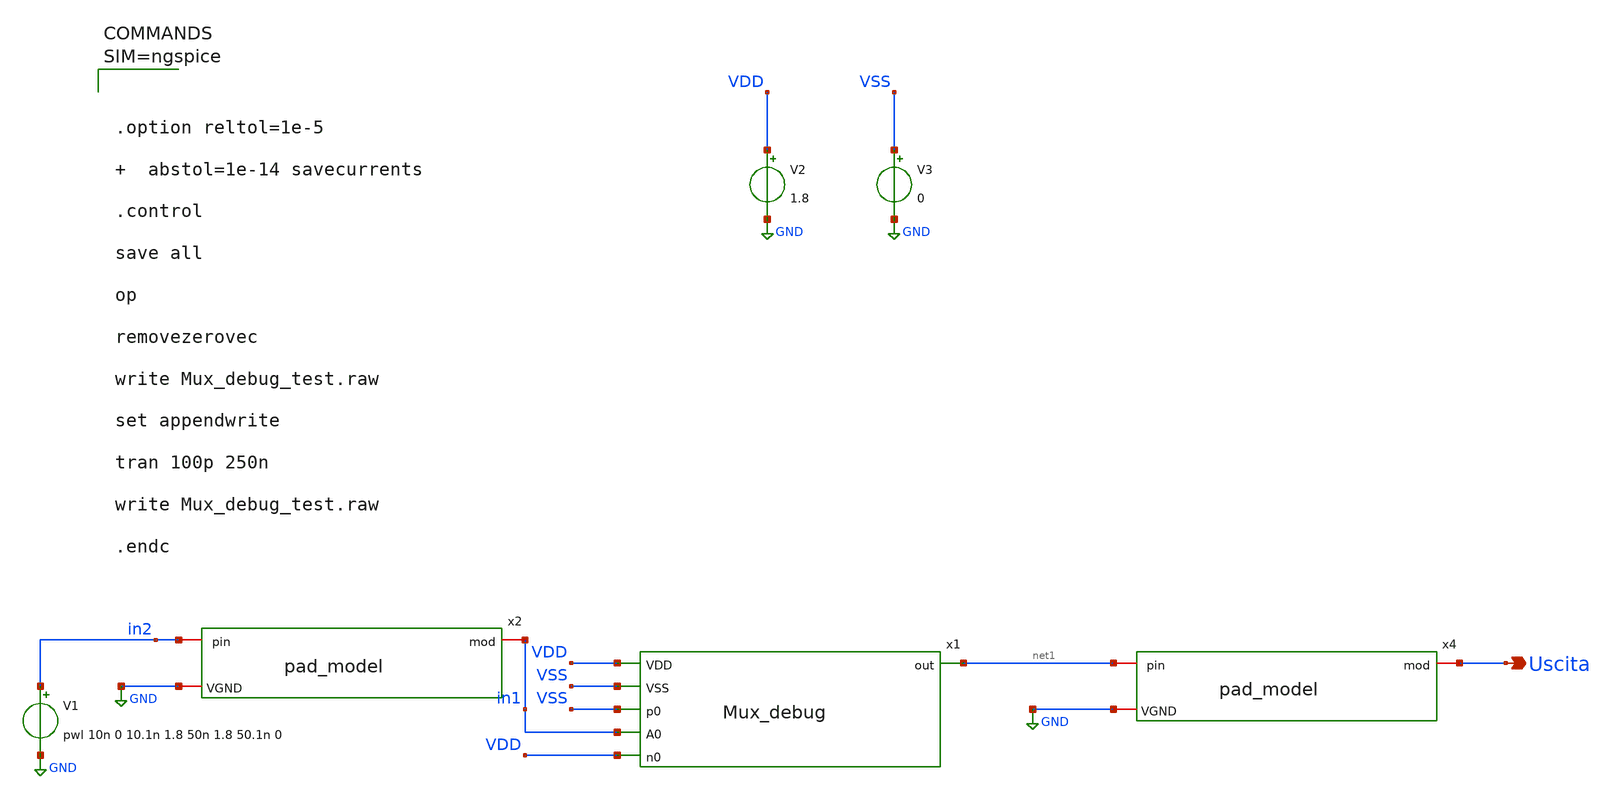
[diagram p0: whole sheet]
** sch_path: xschem/Utili/Mux_debug_test.sch
**.subckt Mux_debug_test Uscita
*.opin Uscita
V1 in2 GND pwl 10n 0 10.1n 1.8 50n 1.8 50.1n 0
x2 GND in2 in1 pad_model
x4 GND net1 Uscita pad_model
x1 VDD VSS VSS net1 in1 VDD Mux_debug
V2 VDD GND 1.8
V3 VSS GND 0
**** begin user architecture code

** opencircuitdesign pdks install
.lib $::SKYWATER_MODELS/sky130.lib.spice tt






.option reltol=1e-5
   abstol=1e-14 savecurrents

.control

save all

op

removezerovec

write Mux_debug_test.raw

set appendwrite

tran 100p 250n

write Mux_debug_test.raw

.endc




**** end user architecture code
**.ends
.GLOBAL GND
.end
